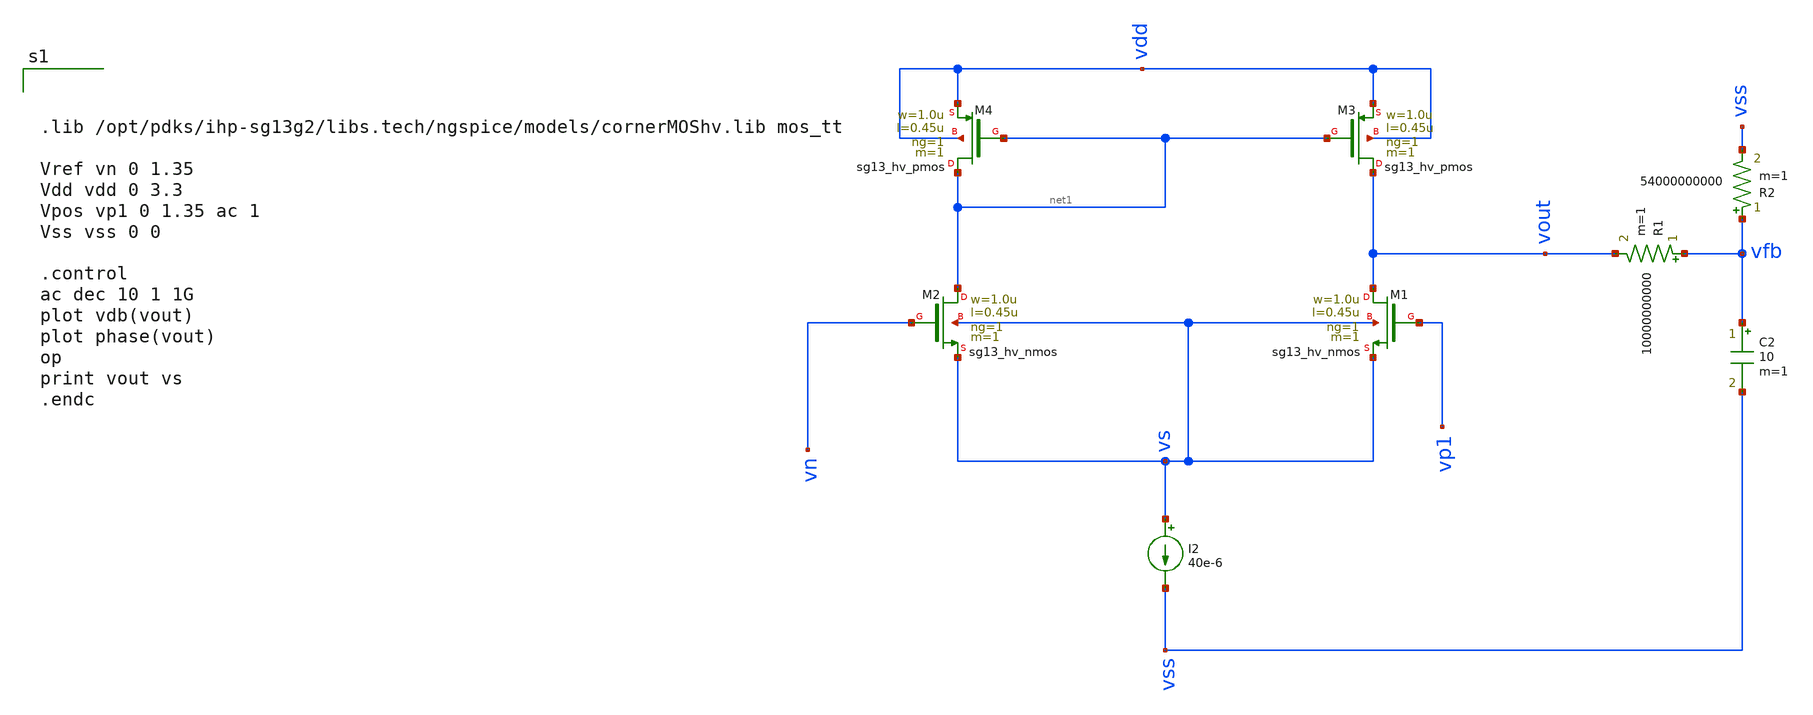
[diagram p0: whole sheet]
** sch_path: test/Tesis_notebooks/xschem/ota_1stage_tb.sch
**.subckt ota_1stage_tb
I2 vs vss 40e-6
XM1 vout vp1 vs vs sg13_hv_nmos w=1.0u l=0.45u ng=1 m=1 mm_ok=1
XM2 net1 vn vs vs sg13_hv_nmos w=1.0u l=0.45u ng=1 m=1 mm_ok=1
XM3 vout net1 vdd vdd sg13_hv_pmos w=1.0u l=0.45u ng=1 m=1 mm_ok=1
XM4 net1 net1 vdd vdd sg13_hv_pmos w=1.0u l=0.45u ng=1 m=1 mm_ok=1
R1 vfb vout 10000000000 m=1
C2 vfb vss 10 m=1
R2 vfb vss 54000000000 m=1
**** begin user architecture code



.lib /opt/pdks/ihp-sg13g2/libs.tech/ngspice/models/cornerMOShv.lib mos_tt

Vref vn 0 1.35
Vdd vdd 0 3.3
Vpos vp1 0 1.35 ac 1
Vss vss 0 0

.control
ac dec 10 1 1G
plot vdb(vout)
plot phase(vout)
op
print vout vs
.endc



**** end user architecture code
**.ends
.end
